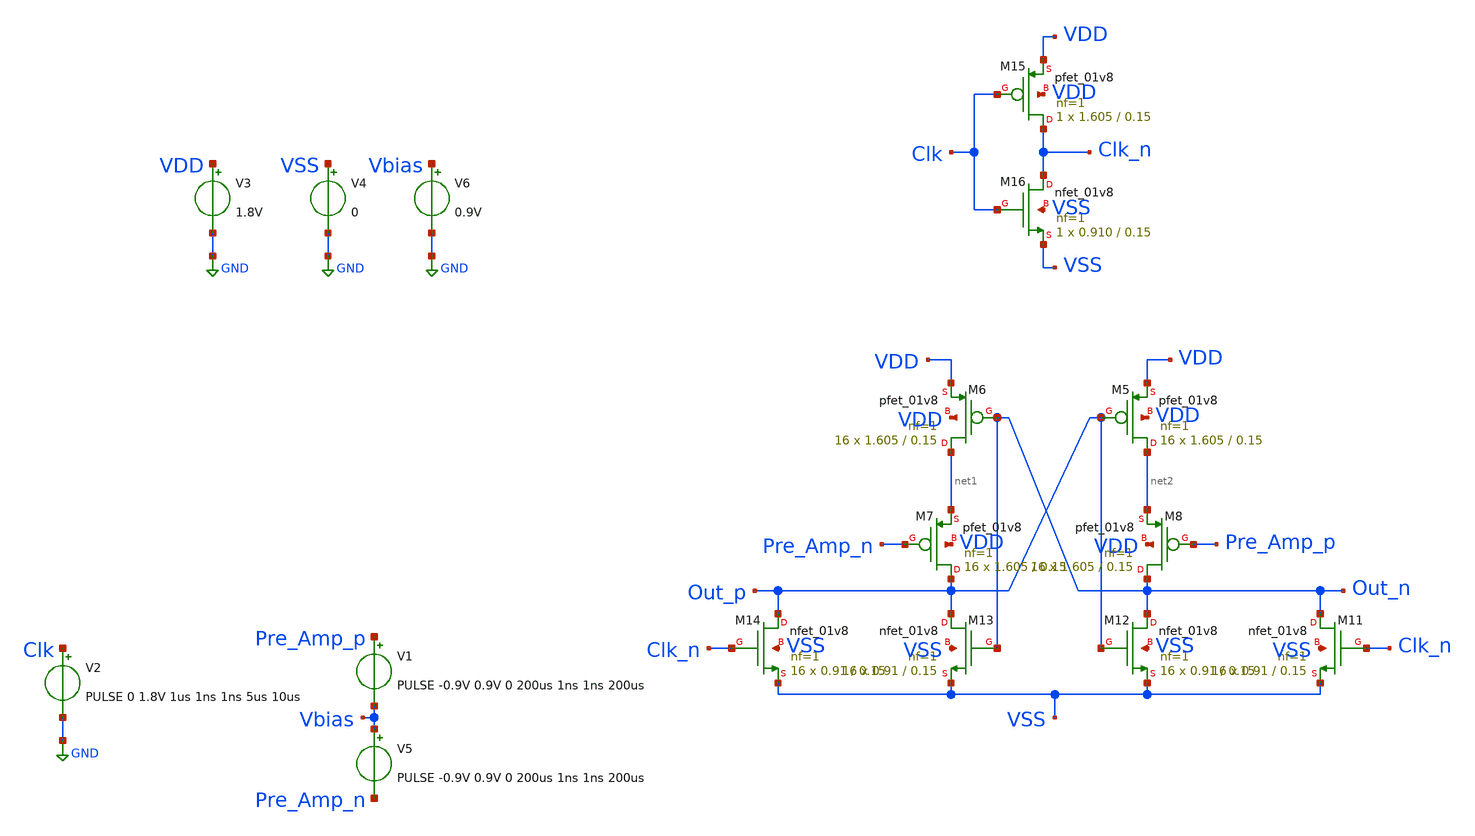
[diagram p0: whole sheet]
** sch_path: xschem/tests/comparator/latch_sandbox.sch
**.subckt latch_sandbox
XM5 net2 Out_p VDD VDD sky130_fd_pr__pfet_01v8 L=0.15 W=1.605 nf=1 ad='int((nf+1)/2) * W/nf * 0.29' as='int((nf+2)/2) * W/nf * 0.29'
+ pd='2*int((nf+1)/2) * (W/nf + 0.29)' ps='2*int((nf+2)/2) * (W/nf + 0.29)' nrd='0.29 / W' nrs='0.29 / W'
+ sa=0 sb=0 sd=0 mult=16 m=16
XM6 net1 Out_n VDD VDD sky130_fd_pr__pfet_01v8 L=0.15 W=1.605 nf=1 ad='int((nf+1)/2) * W/nf * 0.29' as='int((nf+2)/2) * W/nf * 0.29'
+ pd='2*int((nf+1)/2) * (W/nf + 0.29)' ps='2*int((nf+2)/2) * (W/nf + 0.29)' nrd='0.29 / W' nrs='0.29 / W'
+ sa=0 sb=0 sd=0 mult=16 m=16
XM11 Out_n Clk_n VSS VSS sky130_fd_pr__nfet_01v8 L=0.15 W=0.91 nf=1 ad='int((nf+1)/2) * W/nf * 0.29'
+ as='int((nf+2)/2) * W/nf * 0.29' pd='2*int((nf+1)/2) * (W/nf + 0.29)' ps='2*int((nf+2)/2) * (W/nf + 0.29)'
+ nrd='0.29 / W' nrs='0.29 / W' sa=0 sb=0 sd=0 mult=16 m=16
XM12 Out_n Out_p VSS VSS sky130_fd_pr__nfet_01v8 L=0.15 W=0.91 nf=1 ad='int((nf+1)/2) * W/nf * 0.29'
+ as='int((nf+2)/2) * W/nf * 0.29' pd='2*int((nf+1)/2) * (W/nf + 0.29)' ps='2*int((nf+2)/2) * (W/nf + 0.29)'
+ nrd='0.29 / W' nrs='0.29 / W' sa=0 sb=0 sd=0 mult=16 m=16
XM13 Out_p Out_n VSS VSS sky130_fd_pr__nfet_01v8 L=0.15 W=0.91 nf=1 ad='int((nf+1)/2) * W/nf * 0.29'
+ as='int((nf+2)/2) * W/nf * 0.29' pd='2*int((nf+1)/2) * (W/nf + 0.29)' ps='2*int((nf+2)/2) * (W/nf + 0.29)'
+ nrd='0.29 / W' nrs='0.29 / W' sa=0 sb=0 sd=0 mult=16 m=16
XM14 Out_p Clk_n VSS VSS sky130_fd_pr__nfet_01v8 L=0.15 W=0.91 nf=1 ad='int((nf+1)/2) * W/nf * 0.29'
+ as='int((nf+2)/2) * W/nf * 0.29' pd='2*int((nf+1)/2) * (W/nf + 0.29)' ps='2*int((nf+2)/2) * (W/nf + 0.29)'
+ nrd='0.29 / W' nrs='0.29 / W' sa=0 sb=0 sd=0 mult=16 m=16
XM7 Out_p Pre_Amp_n net1 VDD sky130_fd_pr__pfet_01v8 L=0.15 W=1.605 nf=1 ad='int((nf+1)/2) * W/nf * 0.29'
+ as='int((nf+2)/2) * W/nf * 0.29' pd='2*int((nf+1)/2) * (W/nf + 0.29)' ps='2*int((nf+2)/2) * (W/nf + 0.29)'
+ nrd='0.29 / W' nrs='0.29 / W' sa=0 sb=0 sd=0 mult=16 m=16
XM8 Out_n Pre_Amp_p net2 VDD sky130_fd_pr__pfet_01v8 L=0.15 W=1.605 nf=1 ad='int((nf+1)/2) * W/nf * 0.29'
+ as='int((nf+2)/2) * W/nf * 0.29' pd='2*int((nf+1)/2) * (W/nf + 0.29)' ps='2*int((nf+2)/2) * (W/nf + 0.29)'
+ nrd='0.29 / W' nrs='0.29 / W' sa=0 sb=0 sd=0 mult=16 m=16
V3 VDD GND 1.8V
V4 VSS GND 0
V6 Vbias GND 0.9V
V1 Pre_Amp_p Vbias PULSE -0.9V 0.9V 0 200us 1ns 1ns 200us
V5 Vbias Pre_Amp_n PULSE -0.9V 0.9V 0 200us 1ns 1ns 200us
XM15 Clk_n Clk VDD VDD sky130_fd_pr__pfet_01v8 L=0.15 W=1.605 nf=1 ad='int((nf+1)/2) * W/nf * 0.29' as='int((nf+2)/2) * W/nf * 0.29'
+ pd='2*int((nf+1)/2) * (W/nf + 0.29)' ps='2*int((nf+2)/2) * (W/nf + 0.29)' nrd='0.29 / W' nrs='0.29 / W'
+ sa=0 sb=0 sd=0 mult=1 m=1
XM16 Clk_n Clk VSS VSS sky130_fd_pr__nfet_01v8 L=0.15 W=0.910 nf=1 ad='int((nf+1)/2) * W/nf * 0.29' as='int((nf+2)/2) * W/nf * 0.29'
+ pd='2*int((nf+1)/2) * (W/nf + 0.29)' ps='2*int((nf+2)/2) * (W/nf + 0.29)' nrd='0.29 / W' nrs='0.29 / W'
+ sa=0 sb=0 sd=0 mult=1 m=1
V2 Clk GND PULSE 0 1.8V 1us 1ns 1ns 5us 10us
**** begin user architecture code
 .lib $::SKYWATER_MODELS/sky130.lib.spice tt
.include $::SKYWATER_STDCELLS/sky130_fd_sc_hd.spice


.options acct list
.temp 25
*vvcc VDD 0 dc 1.8
*vvss VSS 0 0
.control
tran 0.1u 200u
*dc V1 0 1.8V 0.1
plot pre_amp_p-pre_amp_n+2 Out_p-Out_n Clk-4
plot pre_amp_p pre_amp_n+2 clk-2
write comparator_test_small_v.raw
.endc


**** end user architecture code
**.ends
.GLOBAL GND
.end
